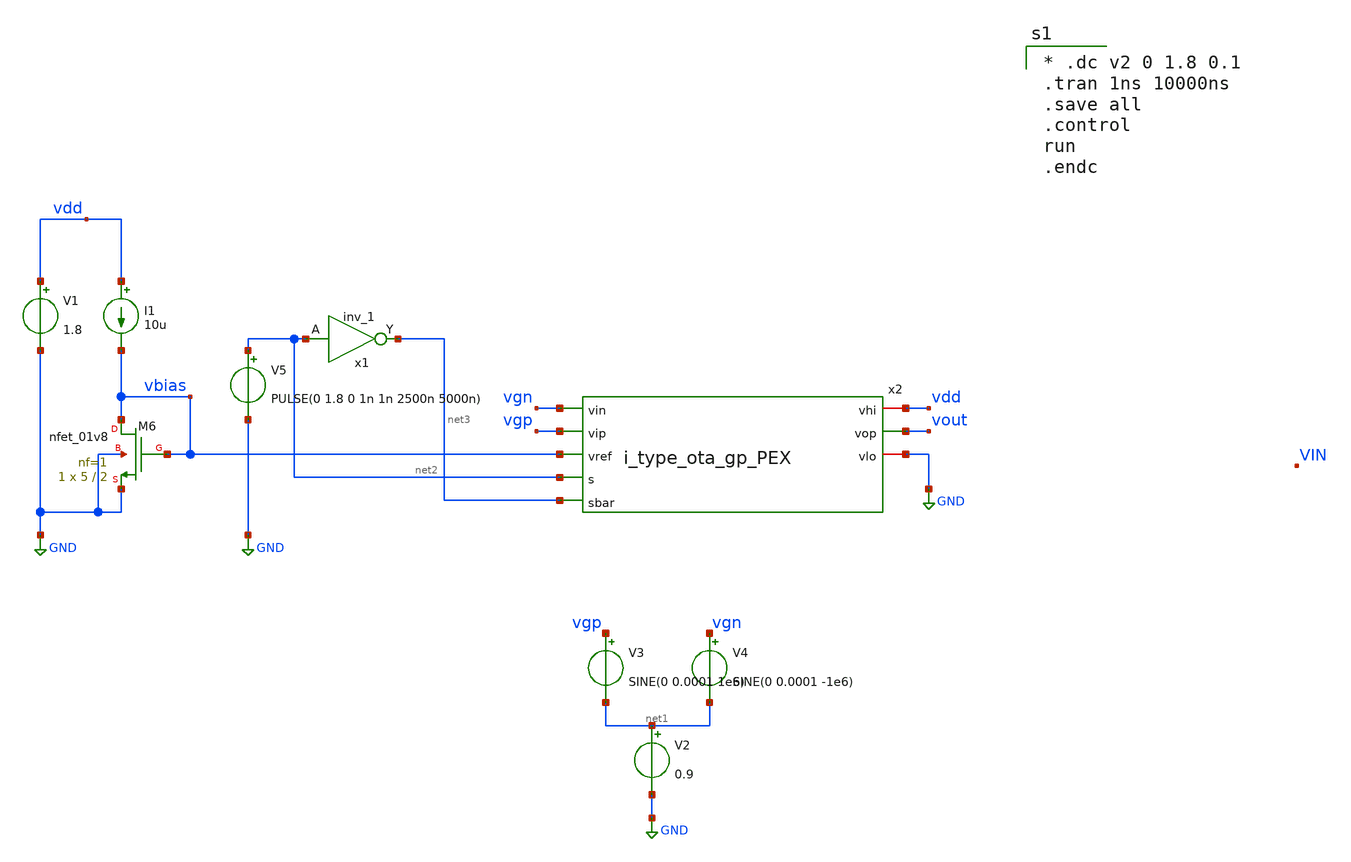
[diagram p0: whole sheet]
** sch_path: xschem/i_type_ota_gp_PEX_tran_tb.sch
**.subckt i_type_ota_gp_PEX_tran_tb
XM6 vbias vbias GND GND sky130_fd_pr__nfet_01v8 L=2 W=5 nf=1 ad='int((nf+1)/2) * W/nf * 0.29' as='int((nf+2)/2) * W/nf * 0.29'
+ pd='2*int((nf+1)/2) * (W/nf + 0.29)' ps='2*int((nf+2)/2) * (W/nf + 0.29)' nrd='0.29 / W' nrs='0.29 / W'
+ sa=0 sb=0 sd=0 mult=1 m=1
I1 vdd vbias 10u
V1 vdd GND 1.8
V2 net1 GND 0.9
V3 vgp net1 SINE(0 0.0001 1e6)
V4 vgn net1 SINE(0 0.0001 -1e6)
x1 net2 gnd gnd vdd vdd net3 sky130_fd_sc_hs__inv_1
V5 net2 GND PULSE(0 1.8 0 1n 1n 2500n 5000n)
x2 vdd vout vgn vgp vbias net2 net3 GND i_type_ota_gp_PEX
**** begin user architecture code
.lib $::SKYWATER_MODELS/sky130.lib.spice tt
.include $::PDKPATH/libs.ref/sky130_fd_sc_hs/spice/sky130_fd_sc_hs.spice


* .dc v2 0 1.8 0.1
.tran 1ns 10000ns
.save all
.control
run
.endc


**** end user architecture code
**.ends

* expanding   symbol:  i_type_ota_gp_PEX.sym # of pins=8
** sym_path: xschem/i_type_ota_gp_PEX.sym
** sch_path: xschem/i_type_ota_gp_PEX.sch
.subckt i_type_ota_gp_PEX vhi vop vin vip vref s sbar vlo
*.ipin vip
*.ipin vin
*.opin vop
*.iopin vhi
*.iopin vlo
*.ipin vref
*.ipin s
*.ipin sbar
**** begin user architecture code

* NGSPICE file created from cmota_1_flat.ext - technology: sky130A

.subckt cmota_gp VHI VLO VREF VIP VIN VOP S SBAR
* NGSPICE file created from cmota_gp.ext - technology: sky130A

X0 gated_iref_0/a_1086_150# S VREF VLO sky130_fd_pr__nfet_01v8 ad=0p pd=0u as=0p ps=0u w=2.5e+06u
+ l=150000u
X1 VLO SBAR gated_iref_0/a_1086_150# VLO sky130_fd_pr__nfet_01v8 ad=0p pd=0u as=0p ps=0u w=2.5e+06u
+ l=150000u
X2 gated_iref_0/a_1086_150# gated_iref_0/OUT VLO sky130_fd_pr__res_xhigh_po w=350000u l=1.49e+06u
X3 VREF S gated_iref_0/a_1086_150# VLO sky130_fd_pr__nfet_01v8 ad=0p pd=0u as=0p ps=0u w=2.5e+06u
+ l=150000u
X4 gated_iref_0/a_1086_150# SBAR VLO VLO sky130_fd_pr__nfet_01v8 ad=0p pd=0u as=0p ps=0u w=2.5e+06u
+ l=150000u
X5 VLO gated_iref_0/OUT sky130_fd_pr__cap_mim_m3_1 l=5.5e+06u w=2.7e+07u
X6 gated_iref_0/OUT VLO sky130_fd_pr__cap_mim_m3_2 l=5.5e+06u w=2.7e+07u
X7 VHI cmota_1_flat_1_0/a_266_188# cmota_1_flat_1_0/a_147_n2312# VHI sky130_fd_pr__pfet_01v8 ad=0p
+ pd=0u as=0p ps=0u w=1e+07u l=300000u
X8 VHI cmota_1_flat_1_0/a_266_188# cmota_1_flat_1_0/a_147_n2312# VHI sky130_fd_pr__pfet_01v8 ad=0p
+ pd=0u as=0p ps=0u w=1e+07u l=300000u
X9 VHI cmota_1_flat_1_0/a_2626_188# VOP VHI sky130_fd_pr__pfet_01v8 ad=0p pd=0u as=0p ps=0u w=1e+07u
+ l=300000u
X10 cmota_1_flat_1_0/a_266_188# VIN gated_iref_0/OUT VLO sky130_fd_pr__nfet_01v8_lvt ad=0p pd=0u
+ as=0p ps=0u w=2.5e+06u l=150000u
X11 VHI cmota_1_flat_1_0/a_2626_188# VOP VHI sky130_fd_pr__pfet_01v8 ad=0p pd=0u as=0p ps=0u
+ w=1e+07u l=300000u
X12 gated_iref_0/OUT VIN cmota_1_flat_1_0/a_266_188# VLO sky130_fd_pr__nfet_01v8_lvt ad=0p pd=0u
+ as=0p ps=0u w=2.5e+06u l=150000u
X13 cmota_1_flat_1_0/a_2626_188# VIP gated_iref_0/OUT VLO sky130_fd_pr__nfet_01v8_lvt ad=0p pd=0u
+ as=0p ps=0u w=2.5e+06u l=150000u
X14 cmota_1_flat_1_0/a_147_n2312# cmota_1_flat_1_0/a_266_188# VHI VHI sky130_fd_pr__pfet_01v8 ad=0p
+ pd=0u as=0p ps=0u w=1e+07u l=300000u
X15 cmota_1_flat_1_0/a_147_n2312# cmota_1_flat_1_0/a_266_188# VHI VHI sky130_fd_pr__pfet_01v8 ad=0p
+ pd=0u as=0p ps=0u w=1e+07u l=300000u
X16 VHI cmota_1_flat_1_0/a_2626_188# VOP VHI sky130_fd_pr__pfet_01v8 ad=0p pd=0u as=0p ps=0u
+ w=1e+07u l=300000u
X17 cmota_1_flat_1_0/a_2626_188# cmota_1_flat_1_0/a_2626_188# VHI VHI sky130_fd_pr__pfet_01v8 ad=0p
+ pd=0u as=0p ps=0u w=1e+07u l=300000u
X18 cmota_1_flat_1_0/a_2626_188# VIP gated_iref_0/OUT VLO sky130_fd_pr__nfet_01v8_lvt ad=0p pd=0u
+ as=0p ps=0u w=2.5e+06u l=150000u
X19 VOP cmota_1_flat_1_0/a_2626_188# VHI VHI sky130_fd_pr__pfet_01v8 ad=0p pd=0u as=0p ps=0u
+ w=1e+07u l=300000u
X20 VLO cmota_1_flat_1_0/a_147_n2312# cmota_1_flat_1_0/a_147_n2312# VLO sky130_fd_pr__nfet_01v8
+ ad=0p pd=0u as=0p ps=0u w=1e+07u l=300000u
X21 cmota_1_flat_1_0/a_147_n2312# cmota_1_flat_1_0/a_147_n2312# VLO VLO sky130_fd_pr__nfet_01v8
+ ad=0p pd=0u as=0p ps=0u w=1e+07u l=300000u
X22 VOP cmota_1_flat_1_0/a_2626_188# VHI VHI sky130_fd_pr__pfet_01v8 ad=0p pd=0u as=0p ps=0u
+ w=1e+07u l=300000u
X23 VOP cmota_1_flat_1_0/a_2626_188# VHI VHI sky130_fd_pr__pfet_01v8 ad=0p pd=0u as=0p ps=0u
+ w=1e+07u l=300000u
X24 VOP cmota_1_flat_1_0/a_2626_188# VHI VHI sky130_fd_pr__pfet_01v8 ad=0p pd=0u as=0p ps=0u
+ w=1e+07u l=300000u
X25 VLO VLO VLO VLO sky130_fd_pr__nfet_01v8 ad=0p pd=0u as=0p ps=0u w=1e+07u l=300000u
X26 gated_iref_0/OUT VLO VLO VLO sky130_fd_pr__nfet_01v8_lvt ad=0p pd=0u as=0p ps=0u w=2.5e+06u
+ l=150000u
X27 VLO cmota_1_flat_1_0/a_147_n2312# VOP VLO sky130_fd_pr__nfet_01v8 ad=0p pd=0u as=0p ps=0u
+ w=1e+07u l=300000u
X28 VHI cmota_1_flat_1_0/a_266_188# cmota_1_flat_1_0/a_147_n2312# VHI sky130_fd_pr__pfet_01v8 ad=0p
+ pd=0u as=0p ps=0u w=1e+07u l=300000u
X29 VOP cmota_1_flat_1_0/a_147_n2312# VLO VLO sky130_fd_pr__nfet_01v8 ad=0p pd=0u as=0p ps=0u
+ w=1e+07u l=300000u
X30 VLO cmota_1_flat_1_0/a_147_n2312# VOP VLO sky130_fd_pr__nfet_01v8 ad=0p pd=0u as=0p ps=0u
+ w=1e+07u l=300000u
X31 VOP cmota_1_flat_1_0/a_147_n2312# VLO VLO sky130_fd_pr__nfet_01v8 ad=0p pd=0u as=0p ps=0u
+ w=1e+07u l=300000u
X32 VHI cmota_1_flat_1_0/a_2626_188# cmota_1_flat_1_0/a_2626_188# VHI sky130_fd_pr__pfet_01v8 ad=0p
+ pd=0u as=0p ps=0u w=1e+07u l=300000u
X33 VHI cmota_1_flat_1_0/a_2626_188# VOP VHI sky130_fd_pr__pfet_01v8 ad=0p pd=0u as=0p ps=0u
+ w=1e+07u l=300000u
X34 gated_iref_0/OUT VIP cmota_1_flat_1_0/a_2626_188# VLO sky130_fd_pr__nfet_01v8_lvt ad=0p pd=0u
+ as=0p ps=0u w=2.5e+06u l=150000u
X35 VLO cmota_1_flat_1_0/VREF gated_iref_0/OUT VLO sky130_fd_pr__nfet_01v8 ad=0p pd=0u as=0p ps=0u
+ w=1e+07u l=2e+06u
X36 cmota_1_flat_1_0/a_147_n2312# cmota_1_flat_1_0/a_266_188# VHI VHI sky130_fd_pr__pfet_01v8 ad=0p
+ pd=0u as=0p ps=0u w=1e+07u l=300000u
X37 cmota_1_flat_1_0/a_147_n2312# cmota_1_flat_1_0/a_266_188# VHI VHI sky130_fd_pr__pfet_01v8 ad=0p
+ pd=0u as=0p ps=0u w=1e+07u l=300000u
X38 VHI cmota_1_flat_1_0/a_2626_188# VOP VHI sky130_fd_pr__pfet_01v8 ad=0p pd=0u as=0p ps=0u
+ w=1e+07u l=300000u
X39 VLO VLO VLO VLO sky130_fd_pr__nfet_01v8_lvt ad=0p pd=0u as=0p ps=0u w=2.5e+06u l=150000u
X40 VLO cmota_1_flat_1_0/VREF gated_iref_0/OUT VLO sky130_fd_pr__nfet_01v8 ad=0p pd=0u as=0p ps=0u
+ w=1e+07u l=2e+06u
X41 VHI VHI VHI VHI sky130_fd_pr__pfet_01v8 ad=0p pd=0u as=0p ps=0u w=1e+07u l=300000u
X42 VHI VHI VHI VHI sky130_fd_pr__pfet_01v8 ad=0p pd=0u as=0p ps=0u w=1e+07u l=300000u
X43 gated_iref_0/OUT VIN cmota_1_flat_1_0/a_266_188# VLO sky130_fd_pr__nfet_01v8_lvt ad=0p pd=0u
+ as=0p ps=0u w=2.5e+06u l=150000u
X44 cmota_1_flat_1_0/a_147_n2312# cmota_1_flat_1_0/a_266_188# VHI VHI sky130_fd_pr__pfet_01v8 ad=0p
+ pd=0u as=0p ps=0u w=1e+07u l=300000u
X45 cmota_1_flat_1_0/a_2626_188# cmota_1_flat_1_0/a_2626_188# VHI VHI sky130_fd_pr__pfet_01v8 ad=0p
+ pd=0u as=0p ps=0u w=1e+07u l=300000u
X46 cmota_1_flat_1_0/a_266_188# cmota_1_flat_1_0/a_266_188# VHI VHI sky130_fd_pr__pfet_01v8 ad=0p
+ pd=0u as=0p ps=0u w=1e+07u l=300000u
X47 VOP cmota_1_flat_1_0/a_2626_188# VHI VHI sky130_fd_pr__pfet_01v8 ad=0p pd=0u as=0p ps=0u
+ w=1e+07u l=300000u
X48 cmota_1_flat_1_0/a_266_188# VIN gated_iref_0/OUT VLO sky130_fd_pr__nfet_01v8_lvt ad=0p pd=0u
+ as=0p ps=0u w=2.5e+06u l=150000u
X49 VLO cmota_1_flat_1_0/a_147_n2312# cmota_1_flat_1_0/a_147_n2312# VLO sky130_fd_pr__nfet_01v8
+ ad=0p pd=0u as=0p ps=0u w=1e+07u l=300000u
X50 gated_iref_0/OUT VIP cmota_1_flat_1_0/a_2626_188# VLO sky130_fd_pr__nfet_01v8_lvt ad=0p pd=0u
+ as=0p ps=0u w=2.5e+06u l=150000u
X51 VHI cmota_1_flat_1_0/a_266_188# cmota_1_flat_1_0/a_147_n2312# VHI sky130_fd_pr__pfet_01v8 ad=0p
+ pd=0u as=0p ps=0u w=1e+07u l=300000u
X52 VHI cmota_1_flat_1_0/a_266_188# cmota_1_flat_1_0/a_147_n2312# VHI sky130_fd_pr__pfet_01v8 ad=0p
+ pd=0u as=0p ps=0u w=1e+07u l=300000u
X53 VOP cmota_1_flat_1_0/a_2626_188# VHI VHI sky130_fd_pr__pfet_01v8 ad=0p pd=0u as=0p ps=0u
+ w=1e+07u l=300000u
X54 VHI VHI VHI VHI sky130_fd_pr__pfet_01v8 ad=0p pd=0u as=0p ps=0u w=1e+07u l=300000u
X55 cmota_1_flat_1_0/a_147_n2312# cmota_1_flat_1_0/a_147_n2312# VLO VLO sky130_fd_pr__nfet_01v8
+ ad=0p pd=0u as=0p ps=0u w=1e+07u l=300000u
X56 VLO cmota_1_flat_1_0/a_147_n2312# cmota_1_flat_1_0/a_147_n2312# VLO sky130_fd_pr__nfet_01v8
+ ad=0p pd=0u as=0p ps=0u w=1e+07u l=300000u
X57 VLO VLO VLO VLO sky130_fd_pr__nfet_01v8 ad=0p pd=0u as=0p ps=0u w=1e+07u l=300000u
X58 VOP cmota_1_flat_1_0/a_147_n2312# VLO VLO sky130_fd_pr__nfet_01v8 ad=0p pd=0u as=0p ps=0u
+ w=1e+07u l=300000u
X59 VLO cmota_1_flat_1_0/a_147_n2312# VOP VLO sky130_fd_pr__nfet_01v8 ad=0p pd=0u as=0p ps=0u
+ w=1e+07u l=300000u
X60 VHI cmota_1_flat_1_0/a_266_188# cmota_1_flat_1_0/a_266_188# VHI sky130_fd_pr__pfet_01v8 ad=0p
+ pd=0u as=0p ps=0u w=1e+07u l=300000u
X61 VLO cmota_1_flat_1_0/a_147_n2312# VOP VLO sky130_fd_pr__nfet_01v8 ad=0p pd=0u as=0p ps=0u
+ w=1e+07u l=300000u
X62 VHI cmota_1_flat_1_0/a_266_188# cmota_1_flat_1_0/a_147_n2312# VHI sky130_fd_pr__pfet_01v8 ad=0p
+ pd=0u as=0p ps=0u w=1e+07u l=300000u
X63 VHI cmota_1_flat_1_0/a_266_188# cmota_1_flat_1_0/a_147_n2312# VHI sky130_fd_pr__pfet_01v8 ad=0p
+ pd=0u as=0p ps=0u w=1e+07u l=300000u
X64 VLO VLO gated_iref_0/OUT VLO sky130_fd_pr__nfet_01v8_lvt ad=0p pd=0u as=0p ps=0u w=2.5e+06u
+ l=150000u
X65 cmota_1_flat_1_0/a_266_188# VIN gated_iref_0/OUT VLO sky130_fd_pr__nfet_01v8_lvt ad=0p pd=0u
+ as=0p ps=0u w=2.5e+06u l=150000u
X66 VHI cmota_1_flat_1_0/a_266_188# cmota_1_flat_1_0/a_266_188# VHI sky130_fd_pr__pfet_01v8 ad=0p
+ pd=0u as=0p ps=0u w=1e+07u l=300000u
X67 VHI cmota_1_flat_1_0/a_2626_188# VOP VHI sky130_fd_pr__pfet_01v8 ad=0p pd=0u as=0p ps=0u
+ w=1e+07u l=300000u
X68 VHI cmota_1_flat_1_0/a_2626_188# VOP VHI sky130_fd_pr__pfet_01v8 ad=0p pd=0u as=0p ps=0u
+ w=1e+07u l=300000u
X69 VLO VLO VLO VLO sky130_fd_pr__nfet_01v8 ad=0p pd=0u as=0p ps=0u w=1e+07u l=300000u
X70 gated_iref_0/OUT cmota_1_flat_1_0/VREF VLO VLO sky130_fd_pr__nfet_01v8 ad=0p pd=0u as=0p ps=0u
+ w=1e+07u l=2e+06u
X71 cmota_1_flat_1_0/a_147_n2312# cmota_1_flat_1_0/a_266_188# VHI VHI sky130_fd_pr__pfet_01v8 ad=0p
+ pd=0u as=0p ps=0u w=1e+07u l=300000u
X72 VLO VLO VLO VLO sky130_fd_pr__nfet_01v8_lvt ad=0p pd=0u as=0p ps=0u w=2.5e+06u l=150000u
X73 gated_iref_0/OUT VIN cmota_1_flat_1_0/a_266_188# VLO sky130_fd_pr__nfet_01v8_lvt ad=0p pd=0u
+ as=0p ps=0u w=2.5e+06u l=150000u
X74 gated_iref_0/OUT cmota_1_flat_1_0/VREF VLO VLO sky130_fd_pr__nfet_01v8 ad=0p pd=0u as=0p ps=0u
+ w=1e+07u l=2e+06u
X75 cmota_1_flat_1_0/a_2626_188# VIP gated_iref_0/OUT VLO sky130_fd_pr__nfet_01v8_lvt ad=0p pd=0u
+ as=0p ps=0u w=2.5e+06u l=150000u
X76 cmota_1_flat_1_0/a_147_n2312# cmota_1_flat_1_0/a_266_188# VHI VHI sky130_fd_pr__pfet_01v8 ad=0p
+ pd=0u as=0p ps=0u w=1e+07u l=300000u
X77 gated_iref_0/OUT VIN cmota_1_flat_1_0/a_266_188# VLO sky130_fd_pr__nfet_01v8_lvt ad=0p pd=0u
+ as=0p ps=0u w=2.5e+06u l=150000u
X78 cmota_1_flat_1_0/a_147_n2312# cmota_1_flat_1_0/a_266_188# VHI VHI sky130_fd_pr__pfet_01v8 ad=0p
+ pd=0u as=0p ps=0u w=1e+07u l=300000u
X79 VOP cmota_1_flat_1_0/a_2626_188# VHI VHI sky130_fd_pr__pfet_01v8 ad=0p pd=0u as=0p ps=0u
+ w=1e+07u l=300000u
X80 cmota_1_flat_1_0/a_2626_188# VIP gated_iref_0/OUT VLO sky130_fd_pr__nfet_01v8_lvt ad=0p pd=0u
+ as=0p ps=0u w=2.5e+06u l=150000u
X81 VLO VLO VLO VLO sky130_fd_pr__nfet_01v8 ad=0p pd=0u as=0p ps=0u w=1e+07u l=300000u
X82 cmota_1_flat_1_0/a_266_188# cmota_1_flat_1_0/a_266_188# VHI VHI sky130_fd_pr__pfet_01v8 ad=0p
+ pd=0u as=0p ps=0u w=1e+07u l=300000u
X83 VOP cmota_1_flat_1_0/a_2626_188# VHI VHI sky130_fd_pr__pfet_01v8 ad=0p pd=0u as=0p ps=0u
+ w=1e+07u l=300000u
X84 cmota_1_flat_1_0/a_147_n2312# cmota_1_flat_1_0/a_147_n2312# VLO VLO sky130_fd_pr__nfet_01v8
+ ad=0p pd=0u as=0p ps=0u w=1e+07u l=300000u
X85 gated_iref_0/OUT VIP cmota_1_flat_1_0/a_2626_188# VLO sky130_fd_pr__nfet_01v8_lvt ad=0p pd=0u
+ as=0p ps=0u w=2.5e+06u l=150000u
X86 cmota_1_flat_1_0/a_147_n2312# cmota_1_flat_1_0/a_147_n2312# VLO VLO sky130_fd_pr__nfet_01v8
+ ad=0p pd=0u as=0p ps=0u w=1e+07u l=300000u
X87 VLO cmota_1_flat_1_0/a_147_n2312# cmota_1_flat_1_0/a_147_n2312# VLO sky130_fd_pr__nfet_01v8
+ ad=0p pd=0u as=0p ps=0u w=1e+07u l=300000u
X88 VOP cmota_1_flat_1_0/a_147_n2312# VLO VLO sky130_fd_pr__nfet_01v8 ad=0p pd=0u as=0p ps=0u
+ w=1e+07u l=300000u
X89 gated_iref_0/OUT VIP cmota_1_flat_1_0/a_2626_188# VLO sky130_fd_pr__nfet_01v8_lvt ad=0p pd=0u
+ as=0p ps=0u w=2.5e+06u l=150000u
X90 VHI VHI VHI VHI sky130_fd_pr__pfet_01v8 ad=0p pd=0u as=0p ps=0u w=1e+07u l=300000u
X91 VHI cmota_1_flat_1_0/a_266_188# cmota_1_flat_1_0/a_147_n2312# VHI sky130_fd_pr__pfet_01v8 ad=0p
+ pd=0u as=0p ps=0u w=1e+07u l=300000u
X92 cmota_1_flat_1_0/a_266_188# VIN gated_iref_0/OUT VLO sky130_fd_pr__nfet_01v8_lvt ad=0p pd=0u
+ as=0p ps=0u w=2.5e+06u l=150000u
X93 VHI cmota_1_flat_1_0/a_2626_188# cmota_1_flat_1_0/a_2626_188# VHI sky130_fd_pr__pfet_01v8 ad=0p
+ pd=0u as=0p ps=0u w=1e+07u l=300000u
X94 VHI cmota_1_flat_1_0/a_2626_188# VOP VHI sky130_fd_pr__pfet_01v8 ad=0p pd=0u as=0p ps=0u
+ w=1e+07u l=300000u
X95 VHI VLO sky130_fd_pr__cap_mim_m3_1 l=3.2e+07u w=1.3e+07u
X96 VLO VHI sky130_fd_pr__cap_mim_m3_2 l=3.2e+07u w=1.3e+07u
C0 VHI VLO 74.47fF
C1 VOP VHI 35.24fF
C2 cmota_1_flat_1_0/VREF gated_iref_0/OUT 3.15fF
C3 cmota_1_flat_1_0/a_266_188# VHI 14.23fF
C4 cmota_1_flat_1_0/a_266_188# cmota_1_flat_1_0/a_147_n2312# 2.70fF
C5 VLO gated_iref_0/OUT 37.58fF
C6 cmota_1_flat_1_0/a_2626_188# VHI 14.15fF
C7 VHI cmota_1_flat_1_0/a_147_n2312# 36.19fF
C8 cmota_1_flat_1_0/a_266_188# gated_iref_0/OUT 6.42fF
C9 VHI gated_iref_0/OUT 4.50fF
C10 cmota_1_flat_1_0/a_2626_188# gated_iref_0/OUT 5.97fF
C11 cmota_1_flat_1_0/a_147_n2312# gated_iref_0/OUT 2.74fF
C12 cmota_1_flat_1_0/VREF 0 7.19fF $ **FLOATING
C13 VOP 0 17.35fF $ **FLOATING
C14 cmota_1_flat_1_0/a_147_n2312# 0 22.96fF $ **FLOATING
C15 VHI 0 52.32fF $ **FLOATING
C16 VLO 0 12.48fF $ **FLOATING
C17 gated_iref_0/OUT 0 12.44fF $ **FLOATING


.ends



XDUT vhi vlo vref vip vin vop s sbar cmota_gp


**** end user architecture code
.ends

.GLOBAL GND
.end
